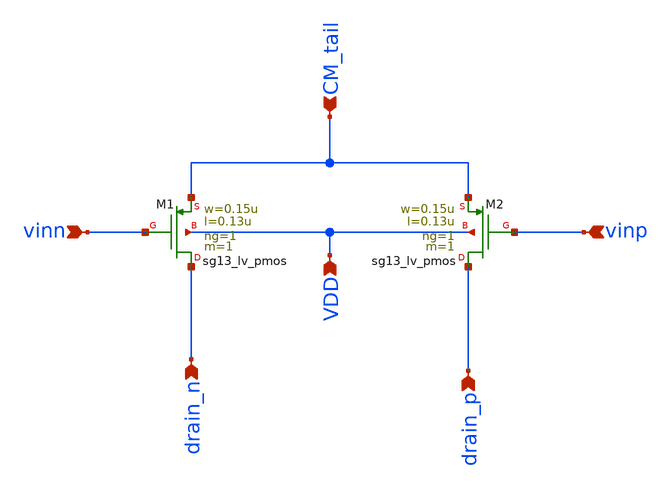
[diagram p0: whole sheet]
** sch_path: analog-db/templates/miscellaneous/diff_pair_pmos.sch
* Copyright 2026 MacAnalog Research Group
**.subckt diff_pair_pmos vinp vinn CM_tail drain_n drain_p VDD
*.ipin vinp
*.ipin vinn
*.ipin CM_tail
*.ipin drain_n
*.ipin drain_p
*.ipin VDD
XM1 drain_n vinn CM_tail VDD sg13_lv_pmos w=0.15u l=0.13u ng=1 m=1 mm_ok=1
XM2 drain_p vinp CM_tail VDD sg13_lv_pmos w=0.15u l=0.13u ng=1 m=1 mm_ok=1
**.ends
.end
